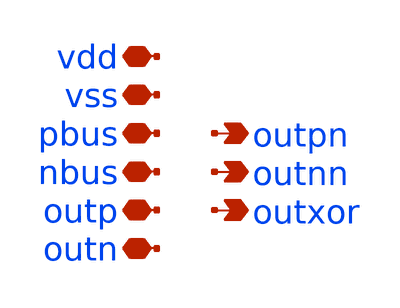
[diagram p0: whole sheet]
** sch_path: xschem/active_load_pex.sch
**.subckt active_load_pex vdd vss pbus nbus outp outn outpn outnn outxor
*.iopin vdd
*.iopin vss
*.iopin pbus
*.iopin nbus
*.iopin outp
*.iopin outn
*.opin outpn
*.opin outnn
*.opin outxor
**** begin user architecture code

* NGSPICE file created from active_load_flat.ext - technology: gf180mcuC

.subckt active_load_flat nbus outn outnn outp outpn outxor pbus vdd vss
X0 vss outn outp vss nfet_06v0 w=0.82u l=0.6u
X1 pbus nbus vdd vdd pfet_06v0 w=1.22u l=0.5u
X2 outp nbus vss vss nfet_06v0 w=0.82u l=0.6u
X3 vdd a_8300_8215# a_8212_8312# vdd pfet_06v0 w=1.22u l=1u
X4 nbus nbus vss vss nfet_06v0 w=0.82u l=0.6u
X5 vdd a_7068_7080# a_6980_7124# vdd pfet_06v0 w=1.22u l=1u
X6 vdd a_9532_8215# a_9444_8312# vdd pfet_06v0 w=1.22u l=1u
X7 pbus nbus vss vss nfet_06v0 w=0.82u l=0.6u
X8 nbus nbus vss vss nfet_06v0 w=0.82u l=0.6u
X9 vdd a_8860_7080# a_8772_7124# vdd pfet_06v0 w=1.22u l=1u
X10 pbus pbus vss vss nfet_06v0 w=0.82u l=0.6u
X11 outxor a_9016_6876# vss vss nfet_06v0 w=0.82u l=0.6u
X12 outn outn vss vss nfet_06v0 w=0.82u l=0.6u
X13 vdd a_8748_5079# a_8660_5176# vdd pfet_06v0 w=1.22u l=1u
X14 nbus nbus vss vss nfet_06v0 w=0.82u l=0.6u
X15 pbus pbus vss vss nfet_06v0 w=0.82u l=0.6u
X16 nbus nbus vss vss nfet_06v0 w=0.82u l=0.6u
X17 outp nbus vss vss nfet_06v0 w=0.82u l=0.6u
X18 vdd a_9980_8215# a_9892_8312# vdd pfet_06v0 w=1.22u l=1u
X19 pbus pbus vss vss nfet_06v0 w=0.82u l=0.6u
X20 pbus pbus vss vss nfet_06v0 w=0.82u l=0.6u
X21 nbus nbus vss vss nfet_06v0 w=0.82u l=0.6u
X22 pbus nbus vss vss nfet_06v0 w=0.82u l=0.6u
X23 a_6956_5512# a_6868_5556# vss vss nfet_06v0 w=0.82u l=1u
X24 nbus pbus vss vss nfet_06v0 w=0.82u l=0.6u
X25 vdd outn outn vdd pfet_06v0 w=1.22u l=0.5u
X26 a_6172_5079# a_6084_5176# vss vss nfet_06v0 w=0.82u l=1u
X27 vdd a_6060_8215# a_5972_8312# vdd pfet_06v0 w=1.22u l=1u
X28 pbus pbus vss vss nfet_06v0 w=0.82u l=0.6u
X29 pbus pbus vss vss nfet_06v0 w=0.82u l=0.6u
X30 a_1692_7080# a_1604_7124# vss vss nfet_06v0 w=0.82u l=1u
X31 pbus pbus vdd vdd pfet_06v0 w=1.22u l=0.5u
X32 a_6508_8215# a_6420_8312# vss vss nfet_06v0 w=0.82u l=1u
X33 nbus pbus vdd vdd pfet_06v0 w=1.22u l=0.5u
X34 a_9912_6340# outpn outxor vss nfet_06v0 w=0.82u l=0.6u
X35 pbus nbus vdd vdd pfet_06v0 w=1.22u l=0.5u
X36 vdd outn outnn vdd pfet_06v0 w=1.22u l=0.5u
X37 a_6956_8215# a_6868_8312# vss vss nfet_06v0 w=0.82u l=1u
X38 a_7516_7080# a_7428_7124# vss vss nfet_06v0 w=0.82u l=1u
X39 a_1692_8215# a_1604_8312# vss vss nfet_06v0 w=0.82u l=1u
X40 vdd a_8860_3944# a_8772_3988# vdd pfet_06v0 w=1.22u l=1u
X41 pbus nbus vdd vdd pfet_06v0 w=1.22u l=0.5u
X42 a_7516_6647# a_7428_6744# vss vss nfet_06v0 w=0.82u l=1u
X43 vdd a_5052_3944# a_4964_3988# vdd pfet_06v0 w=1.22u l=1u
X44 nbus nbus vdd vdd pfet_06v0 w=1.22u l=0.5u
X45 nbus nbus vss vss nfet_06v0 w=0.82u l=0.6u
X46 pbus pbus vdd vdd pfet_06v0 w=1.22u l=0.5u
X47 nbus nbus vdd vdd pfet_06v0 w=1.22u l=0.5u
X48 a_5612_8215# a_5524_8312# vss vss nfet_06v0 w=0.82u l=1u
X49 a_7964_7080# a_7876_7124# vss vss nfet_06v0 w=0.82u l=1u
X50 nbus nbus vss vss nfet_06v0 w=0.82u l=0.6u
X51 nbus nbus vdd vdd pfet_06v0 w=1.22u l=0.5u
X52 nbus nbus vss vss nfet_06v0 w=0.82u l=0.6u
X53 nbus nbus vdd vdd pfet_06v0 w=1.22u l=0.5u
X54 a_7964_6647# a_7876_6744# vss vss nfet_06v0 w=0.82u l=1u
X55 vss outnn a_9912_6340# vss nfet_06v0 w=0.82u l=0.6u
X56 a_8748_8215# a_8660_8312# vss vss nfet_06v0 w=0.82u l=1u
X57 a_6620_7080# a_6532_7124# vss vss nfet_06v0 w=0.82u l=1u
X58 pbus pbus vss vss nfet_06v0 w=0.82u l=0.6u
X59 outn pbus vss vss nfet_06v0 w=0.82u l=0.6u
X60 nbus nbus vss vss nfet_06v0 w=0.82u l=0.6u
X61 outp nbus vss vss nfet_06v0 w=0.82u l=0.6u
X62 outp outp vss vss nfet_06v0 w=0.82u l=0.6u
X63 outn pbus vdd vdd pfet_06v0 w=1.22u l=0.5u
X64 vdd a_6172_5079# a_6084_5176# vdd pfet_06v0 w=1.22u l=1u
X65 pbus pbus vss vss nfet_06v0 w=0.82u l=0.6u
X66 nbus pbus vss vss nfet_06v0 w=0.82u l=0.6u
X67 vdd a_6956_5512# a_6868_5556# vdd pfet_06v0 w=1.22u l=1u
X68 outp nbus vss vss nfet_06v0 w=0.82u l=0.6u
X69 nbus nbus vss vss nfet_06v0 w=0.82u l=0.6u
X70 a_7404_8215# a_7316_8312# vss vss nfet_06v0 w=0.82u l=1u
X71 outp outp vdd vdd pfet_06v0 w=1.22u l=0.5u
X72 pbus pbus vdd vdd pfet_06v0 w=1.22u l=0.5u
X73 outxor outpn a_9688_6744# vdd pfet_06v0 w=1.22u l=0.5u
X74 nbus nbus vss vss nfet_06v0 w=0.82u l=0.6u
X75 nbus nbus vdd vdd pfet_06v0 w=1.22u l=0.5u
X76 outp outp vdd vdd pfet_06v0 w=1.22u l=0.5u
X77 nbus nbus vss vss nfet_06v0 w=0.82u l=0.6u
X78 pbus pbus vss vss nfet_06v0 w=0.82u l=0.6u
X79 nbus nbus vdd vdd pfet_06v0 w=1.22u l=0.5u
X80 outp outn vdd vdd pfet_06v0 w=1.22u l=0.5u
X81 a_8860_5512# a_8772_5556# vss vss nfet_06v0 w=0.82u l=1u
X82 a_7852_8215# a_7764_8312# vss vss nfet_06v0 w=0.82u l=1u
X83 a_8412_7080# a_8324_7124# vss vss nfet_06v0 w=0.82u l=1u
X84 vdd a_7516_6647# a_7428_6744# vdd pfet_06v0 w=1.22u l=1u
X85 nbus pbus vdd vdd pfet_06v0 w=1.22u l=0.5u
X86 outn outn vss vss nfet_06v0 w=0.82u l=0.6u
X87 vss outpn a_9016_6876# vss nfet_06v0 w=0.36u l=0.6u
X88 vss nbus pbus vss nfet_06v0 w=0.82u l=0.6u
X89 a_7068_7080# a_6980_7124# vss vss nfet_06v0 w=0.82u l=1u
X90 pbus pbus vss vss nfet_06v0 w=0.82u l=0.6u
X91 vdd a_7964_6647# a_7876_6744# vdd pfet_06v0 w=1.22u l=1u
X92 a_8860_7080# a_8772_7124# vss vss nfet_06v0 w=0.82u l=1u
X93 vdd pbus pbus vdd pfet_06v0 w=1.22u l=0.5u
X94 a_9204_6876# outnn a_9016_6876# vdd pfet_06v0 w=0.56u l=0.5u
X95 nbus nbus vdd vdd pfet_06v0 w=1.22u l=0.5u
X96 pbus pbus vss vss nfet_06v0 w=0.82u l=0.6u
X97 vdd pbus pbus vdd pfet_06v0 w=1.22u l=0.5u
X98 a_9532_3511# a_9444_3608# vss vss nfet_06v0 w=0.82u l=1u
X99 nbus pbus vdd vdd pfet_06v0 w=1.22u l=0.5u
X100 nbus pbus vdd vdd pfet_06v0 w=1.22u l=0.5u
X101 a_8300_8215# a_8212_8312# vss vss nfet_06v0 w=0.82u l=1u
X102 outn outp vss vss nfet_06v0 w=0.82u l=0.6u
X103 a_6172_3511# a_6084_3608# vss vss nfet_06v0 w=0.82u l=1u
X104 outn outn vdd vdd pfet_06v0 w=1.22u l=0.5u
X105 a_9532_8215# a_9444_8312# vss vss nfet_06v0 w=0.82u l=1u
X106 nbus pbus vdd vdd pfet_06v0 w=1.22u l=0.5u
X107 outn pbus vdd vdd pfet_06v0 w=1.22u l=0.5u
X108 pbus pbus vss vss nfet_06v0 w=0.82u l=0.6u
X109 vdd nbus pbus vdd pfet_06v0 w=1.22u l=0.5u
X110 pbus nbus vss vss nfet_06v0 w=0.82u l=0.6u
X111 a_9980_8215# a_9892_8312# vss vss nfet_06v0 w=0.82u l=1u
X112 nbus pbus vss vss nfet_06v0 w=0.82u l=0.6u
X113 outn pbus vdd vdd pfet_06v0 w=1.22u l=0.5u
X114 outn outp vss vss nfet_06v0 w=0.82u l=0.6u
X115 outn outn vdd vdd pfet_06v0 w=1.22u l=0.5u
X116 pbus pbus vss vss nfet_06v0 w=0.82u l=0.6u
X117 nbus nbus vdd vdd pfet_06v0 w=1.22u l=0.5u
X118 a_9688_6744# a_9016_6876# vdd vdd pfet_06v0 w=1.22u l=0.5u
X119 pbus nbus vss vss nfet_06v0 w=0.82u l=0.6u
X120 vdd outn outp vdd pfet_06v0 w=1.22u l=0.5u
X121 pbus pbus vdd vdd pfet_06v0 w=1.22u l=0.5u
X122 outp outp vdd vdd pfet_06v0 w=1.22u l=0.5u
X123 vss outp outpn vss nfet_06v0 w=0.82u l=0.6u
X124 pbus pbus vdd vdd pfet_06v0 w=1.22u l=0.5u
X125 vdd a_9532_3511# a_9444_3608# vdd pfet_06v0 w=1.22u l=1u
X126 pbus pbus vdd vdd pfet_06v0 w=1.22u l=0.5u
X127 vdd a_8860_5512# a_8772_5556# vdd pfet_06v0 w=1.22u l=1u
X128 a_6060_8215# a_5972_8312# vss vss nfet_06v0 w=0.82u l=1u
X129 outn pbus vss vss nfet_06v0 w=0.82u l=0.6u
X130 outp nbus vdd vdd pfet_06v0 w=1.22u l=0.5u
X131 outp nbus vdd vdd pfet_06v0 w=1.22u l=0.5u
X132 vdd a_6508_8215# a_6420_8312# vdd pfet_06v0 w=1.22u l=1u
X133 vdd a_6172_3511# a_6084_3608# vdd pfet_06v0 w=1.22u l=1u
X134 pbus nbus vdd vdd pfet_06v0 w=1.22u l=0.5u
X135 pbus pbus vdd vdd pfet_06v0 w=1.22u l=0.5u
X136 pbus pbus vdd vdd pfet_06v0 w=1.22u l=0.5u
X137 pbus pbus vdd vdd pfet_06v0 w=1.22u l=0.5u
X138 vdd a_6956_8215# a_6868_8312# vdd pfet_06v0 w=1.22u l=1u
X139 pbus pbus vdd vdd pfet_06v0 w=1.22u l=0.5u
X140 pbus pbus vdd vdd pfet_06v0 w=1.22u l=0.5u
X141 nbus nbus vdd vdd pfet_06v0 w=1.22u l=0.5u
X142 vdd a_1692_8215# a_1604_8312# vdd pfet_06v0 w=1.22u l=1u
X143 pbus pbus vss vss nfet_06v0 w=0.82u l=0.6u
X144 pbus nbus vdd vdd pfet_06v0 w=1.22u l=0.5u
X145 vdd a_5612_8215# a_5524_8312# vdd pfet_06v0 w=1.22u l=1u
X146 vdd a_1692_7080# a_1604_7124# vdd pfet_06v0 w=1.22u l=1u
X147 outp outp vss vss nfet_06v0 w=0.82u l=0.6u
X148 a_9016_6876# outnn vss vss nfet_06v0 w=0.36u l=0.6u
X149 a_1692_5079# a_1604_5176# vss vss nfet_06v0 w=0.82u l=1u
X150 outp outn vss vss nfet_06v0 w=0.82u l=0.6u
X151 nbus nbus vss vss nfet_06v0 w=0.82u l=0.6u
X152 vdd a_8748_8215# a_8660_8312# vdd pfet_06v0 w=1.22u l=1u
X153 vdd a_7516_7080# a_7428_7124# vdd pfet_06v0 w=1.22u l=1u
X154 nbus nbus vss vss nfet_06v0 w=0.82u l=0.6u
X155 vdd outp outpn vdd pfet_06v0 w=1.22u l=0.5u
X156 a_9688_6744# outnn outxor vdd pfet_06v0 w=1.22u l=0.5u
X157 vdd a_7404_8215# a_7316_8312# vdd pfet_06v0 w=1.22u l=1u
X158 vss pbus pbus vss nfet_06v0 w=0.82u l=0.6u
X159 a_8748_5079# a_8660_5176# vss vss nfet_06v0 w=0.82u l=1u
X160 pbus nbus vss vss nfet_06v0 w=0.82u l=0.6u
X161 vdd a_7964_7080# a_7876_7124# vdd pfet_06v0 w=1.22u l=1u
X162 outn pbus vdd vdd pfet_06v0 w=1.22u l=0.5u
X163 vss pbus pbus vss nfet_06v0 w=0.82u l=0.6u
X164 outp outp vdd vdd pfet_06v0 w=1.22u l=0.5u
X165 nbus pbus vss vss nfet_06v0 w=0.82u l=0.6u
X166 vdd a_7852_8215# a_7764_8312# vdd pfet_06v0 w=1.22u l=1u
X167 nbus pbus vss vss nfet_06v0 w=0.82u l=0.6u
X168 vdd a_6620_7080# a_6532_7124# vdd pfet_06v0 w=1.22u l=1u
X169 outn outp vdd vdd pfet_06v0 w=1.22u l=0.5u
X170 nbus pbus vss vss nfet_06v0 w=0.82u l=0.6u
X171 outn pbus vss vss nfet_06v0 w=0.82u l=0.6u
X172 nbus nbus vdd vdd pfet_06v0 w=1.22u l=0.5u
X173 pbus pbus vdd vdd pfet_06v0 w=1.22u l=0.5u
X174 outn outn vss vss nfet_06v0 w=0.82u l=0.6u
X175 nbus nbus vdd vdd pfet_06v0 w=1.22u l=0.5u
X176 vdd outpn a_9204_6876# vdd pfet_06v0 w=0.56u l=0.5u
X177 outn pbus vss vss nfet_06v0 w=0.82u l=0.6u
X178 outp outp vss vss nfet_06v0 w=0.82u l=0.6u
X179 nbus nbus vdd vdd pfet_06v0 w=1.22u l=0.5u
X180 nbus nbus vss vss nfet_06v0 w=0.82u l=0.6u
X181 nbus nbus vdd vdd pfet_06v0 w=1.22u l=0.5u
X182 vss outn outnn vss nfet_06v0 w=0.82u l=0.6u
X183 outn outn vdd vdd pfet_06v0 w=1.22u l=0.5u
X184 outp outp vss vss nfet_06v0 w=0.82u l=0.6u
X185 vdd a_1692_5079# a_1604_5176# vdd pfet_06v0 w=1.22u l=1u
X186 outp nbus vdd vdd pfet_06v0 w=1.22u l=0.5u
X187 nbus nbus vdd vdd pfet_06v0 w=1.22u l=0.5u
X188 nbus nbus vss vss nfet_06v0 w=0.82u l=0.6u
X189 nbus nbus vdd vdd pfet_06v0 w=1.22u l=0.5u
X190 vss outn outn vss nfet_06v0 w=0.82u l=0.6u
X191 outn outp vdd vdd pfet_06v0 w=1.22u l=0.5u
X192 a_8860_3944# a_8772_3988# vss vss nfet_06v0 w=0.82u l=1u
X193 a_5052_3944# a_4964_3988# vss vss nfet_06v0 w=0.82u l=1u
X194 nbus pbus vdd vdd pfet_06v0 w=1.22u l=0.5u
X195 pbus pbus vdd vdd pfet_06v0 w=1.22u l=0.5u
X196 nbus nbus vdd vdd pfet_06v0 w=1.22u l=0.5u
X197 vdd a_8412_7080# a_8324_7124# vdd pfet_06v0 w=1.22u l=1u
X198 pbus pbus vdd vdd pfet_06v0 w=1.22u l=0.5u
X199 outp nbus vdd vdd pfet_06v0 w=1.22u l=0.5u
C0 pbus vdd 5.47fF
C1 vdd outn 2.39fF
C2 vdd nbus 5.46fF
C3 vdd outp 2.79fF
C4 pbus nbus 4.17fF
C5 outp outn 2.09fF
C6 outp vss 6.09fF
C7 outn vss 5.91fF
C8 pbus vss 16.82fF
C9 nbus vss 16.68fF
C10 vdd vss 101.68fF
.ends



XDUT nbus outn outnn outp outpn outxor pbus vdd vss active_load_flat


**** end user architecture code
**.ends
.end
